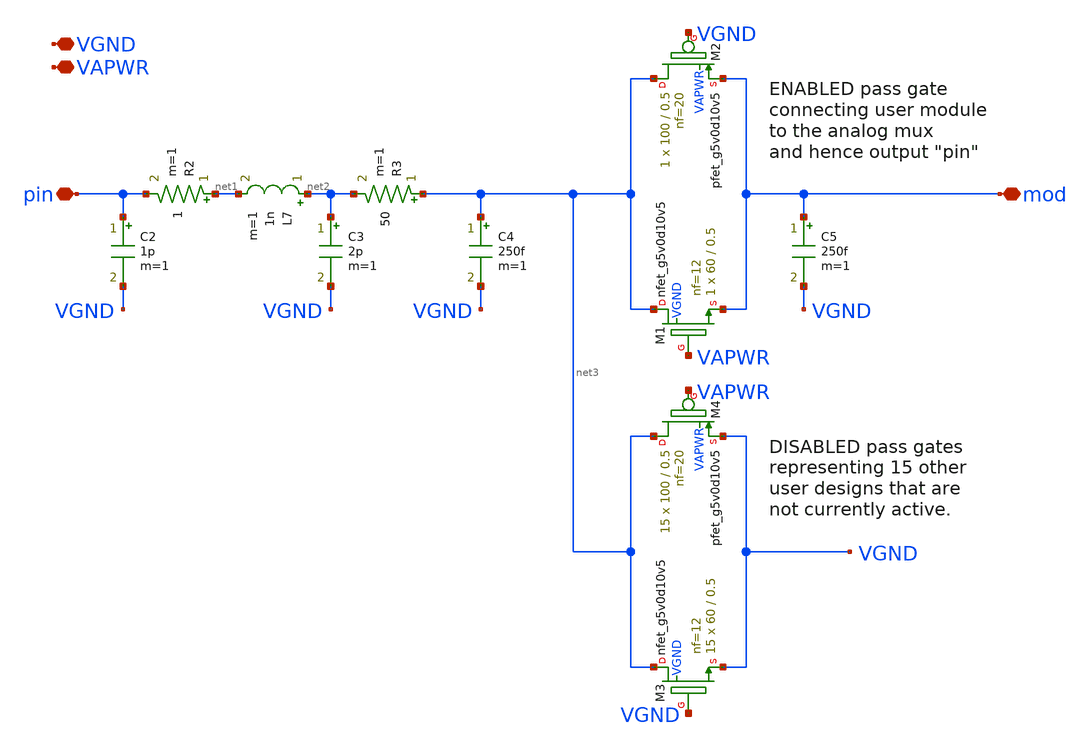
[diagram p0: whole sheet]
** sch_path: xschem/tt_pin_model.sch
**.subckt tt_pin_model VGND VAPWR mod pin
*.iopin VGND
*.iopin VAPWR
*.iopin mod
*.iopin pin
R2 net1 pin 1 m=1
C2 pin VGND 1p m=1
L7 net2 net1 1n m=1
C3 net2 VGND 2p m=1
R3 net3 net2 50 m=1
C4 net3 VGND 250f m=1
XM2 net3 VGND mod VAPWR sky130_fd_pr__pfet_g5v0d10v5 L=0.5 W=100 nf=20 ad='int((nf+1)/2) * W/nf * 0.29'
+ as='int((nf+2)/2) * W/nf * 0.29' pd='2*int((nf+1)/2) * (W/nf + 0.29)' ps='2*int((nf+2)/2) * (W/nf + 0.29)'
+ nrd='0.29 / W' nrs='0.29 / W' sa=0 sb=0 sd=0 mult=1 m=1
XM1 net3 VAPWR mod VGND sky130_fd_pr__nfet_g5v0d10v5 L=0.5 W=60 nf=12 ad='int((nf+1)/2) * W/nf * 0.29'
+ as='int((nf+2)/2) * W/nf * 0.29' pd='2*int((nf+1)/2) * (W/nf + 0.29)' ps='2*int((nf+2)/2) * (W/nf + 0.29)'
+ nrd='0.29 / W' nrs='0.29 / W' sa=0 sb=0 sd=0 mult=1 m=1
XM4 net3 VAPWR VGND VAPWR sky130_fd_pr__pfet_g5v0d10v5 L=0.5 W=100 nf=20 ad='int((nf+1)/2) * W/nf * 0.29'
+ as='int((nf+2)/2) * W/nf * 0.29' pd='2*int((nf+1)/2) * (W/nf + 0.29)' ps='2*int((nf+2)/2) * (W/nf + 0.29)'
+ nrd='0.29 / W' nrs='0.29 / W' sa=0 sb=0 sd=0 mult=15 m=15
XM3 net3 VGND VGND VGND sky130_fd_pr__nfet_g5v0d10v5 L=0.5 W=60 nf=12 ad='int((nf+1)/2) * W/nf * 0.29'
+ as='int((nf+2)/2) * W/nf * 0.29' pd='2*int((nf+1)/2) * (W/nf + 0.29)' ps='2*int((nf+2)/2) * (W/nf + 0.29)'
+ nrd='0.29 / W' nrs='0.29 / W' sa=0 sb=0 sd=0 mult=15 m=15
C5 mod VGND 250f m=1
**.ends
.end
